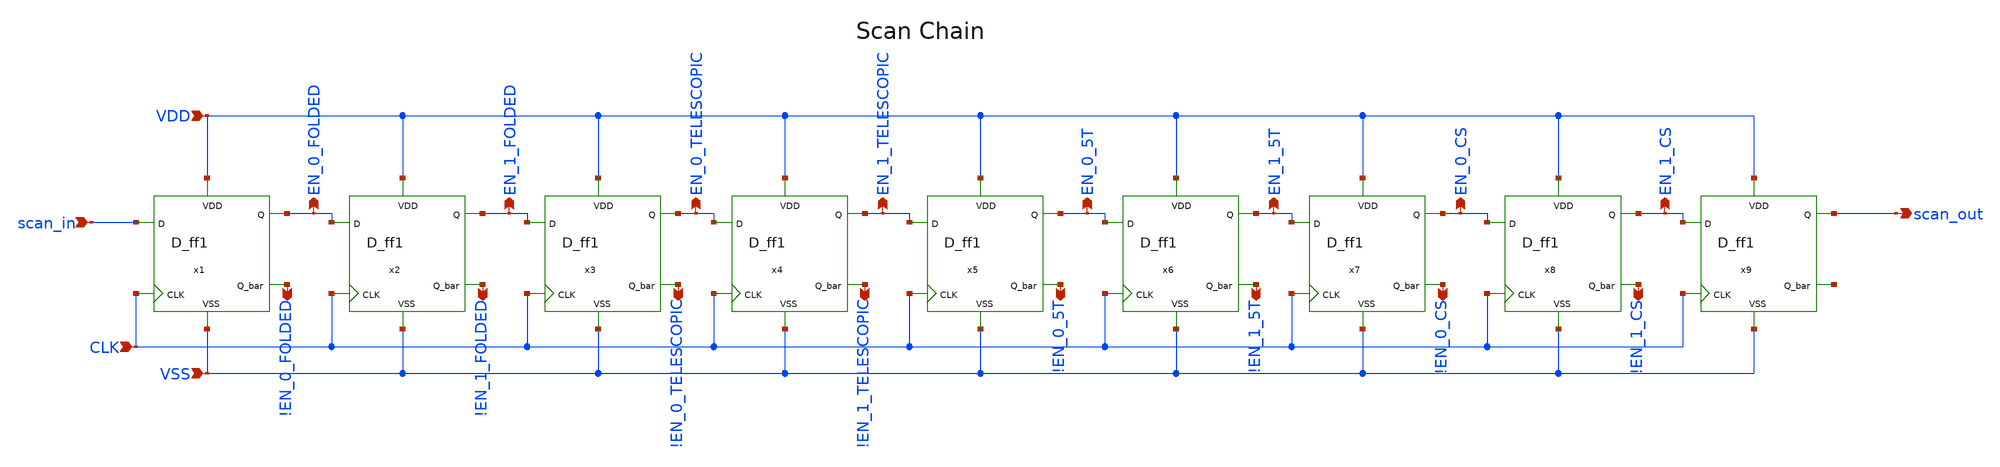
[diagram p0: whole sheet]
** sch_path: designs/libs/core_digital/schem/scan_chain.sch
**.subckt scan_chain scan_in CLK VSS VDD !EN_0_FOLDED !EN_0_TELESCOPIC !EN_1_FOLDED !EN_1_TELESCOPIC
*+ !EN_0_5T !EN_1_5T !EN_0_CS !EN_1_CS scan_out EN_1_CS EN_0_CS EN_1_5T EN_0_5T EN_1_TELESCOPIC EN_0_TELESCOPIC
*+ EN_1_FOLDED EN_0_FOLDED
*.ipin scan_in
*.ipin CLK
*.ipin VSS
*.ipin VDD
*.opin !EN_0_FOLDED
*.opin !EN_0_TELESCOPIC
*.opin !EN_1_FOLDED
*.opin !EN_1_TELESCOPIC
*.opin !EN_0_5T
*.opin !EN_1_5T
*.opin !EN_0_CS
*.opin !EN_1_CS
*.opin scan_out
*.opin EN_1_CS
*.opin EN_0_CS
*.opin EN_1_5T
*.opin EN_0_5T
*.opin EN_1_TELESCOPIC
*.opin EN_0_TELESCOPIC
*.opin EN_1_FOLDED
*.opin EN_0_FOLDED
x1 VDD scan_in EN_0_FOLDED !EN_0_FOLDED CLK VSS D_ff1
x2 VDD EN_0_FOLDED EN_1_FOLDED !EN_1_FOLDED CLK VSS D_ff1
x3 VDD EN_1_FOLDED EN_0_TELESCOPIC !EN_0_TELESCOPIC CLK VSS D_ff1
x4 VDD EN_0_TELESCOPIC EN_1_TELESCOPIC !EN_1_TELESCOPIC CLK VSS D_ff1
x5 VDD EN_1_TELESCOPIC EN_0_5T !EN_0_5T CLK VSS D_ff1
x6 VDD EN_0_5T EN_1_5T !EN_1_5T CLK VSS D_ff1
x7 VDD EN_1_5T EN_0_CS !EN_0_CS CLK VSS D_ff1
x8 VDD EN_0_CS EN_1_CS !EN_1_CS CLK VSS D_ff1
x9 VDD EN_1_CS scan_out net1 CLK VSS D_ff1
**.ends
.end
